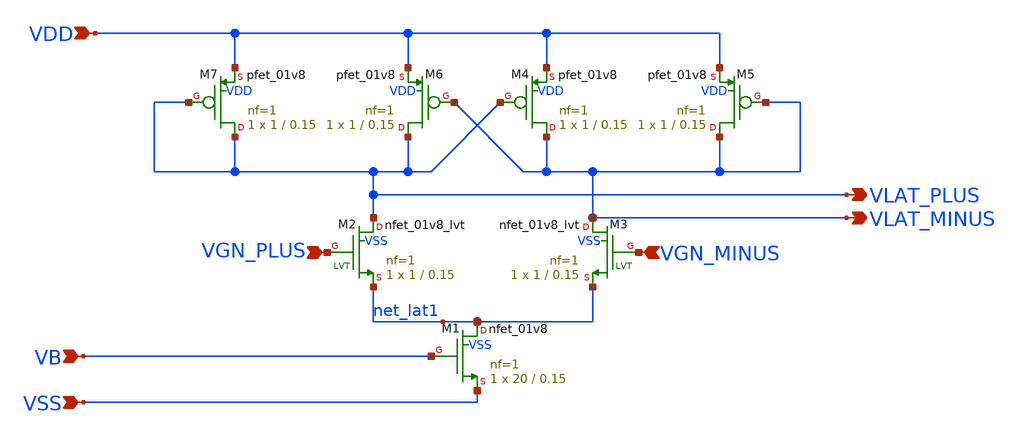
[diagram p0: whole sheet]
** sch_path: xschem/latch.sch
**.subckt latch VDD VSS VGN_PLUS VGN_MINUS VB VLAT_PLUS VLAT_MINUS
*.ipin VDD
*.ipin VSS
*.ipin VGN_PLUS
*.ipin VGN_MINUS
*.ipin VB
*.opin VLAT_PLUS
*.opin VLAT_MINUS
XM1 net_lat1 VB VSS VSS sky130_fd_pr__nfet_01v8 L=0.15 W=20 nf=1 ad='int((nf+1)/2) * W/nf * 0.29' as='int((nf+2)/2) * W/nf * 0.29'
+ pd='2*int((nf+1)/2) * (W/nf + 0.29)' ps='2*int((nf+2)/2) * (W/nf + 0.29)' nrd='0.29 / W' nrs='0.29 / W'
+ sa=0 sb=0 sd=0 mult=1 m=1
XM2 VLAT_PLUS VGN_PLUS net_lat1 VSS sky130_fd_pr__nfet_01v8_lvt L=0.15 W=1 nf=1 ad='int((nf+1)/2) * W/nf * 0.29'
+ as='int((nf+2)/2) * W/nf * 0.29' pd='2*int((nf+1)/2) * (W/nf + 0.29)' ps='2*int((nf+2)/2) * (W/nf + 0.29)'
+ nrd='0.29 / W' nrs='0.29 / W' sa=0 sb=0 sd=0 mult=1 m=1
XM3 VLAT_MINUS VGN_MINUS net_lat1 VSS sky130_fd_pr__nfet_01v8_lvt L=0.15 W=1 nf=1 ad='int((nf+1)/2) * W/nf * 0.29'
+ as='int((nf+2)/2) * W/nf * 0.29' pd='2*int((nf+1)/2) * (W/nf + 0.29)' ps='2*int((nf+2)/2) * (W/nf + 0.29)'
+ nrd='0.29 / W' nrs='0.29 / W' sa=0 sb=0 sd=0 mult=1 m=1
XM4 VLAT_MINUS VLAT_PLUS VDD VDD sky130_fd_pr__pfet_01v8 L=0.15 W=1 nf=1 ad='int((nf+1)/2) * W/nf * 0.29'
+ as='int((nf+2)/2) * W/nf * 0.29' pd='2*int((nf+1)/2) * (W/nf + 0.29)' ps='2*int((nf+2)/2) * (W/nf + 0.29)'
+ nrd='0.29 / W' nrs='0.29 / W' sa=0 sb=0 sd=0 mult=1 m=1
XM5 VLAT_MINUS VLAT_MINUS VDD VDD sky130_fd_pr__pfet_01v8 L=0.15 W=1 nf=1 ad='int((nf+1)/2) * W/nf * 0.29'
+ as='int((nf+2)/2) * W/nf * 0.29' pd='2*int((nf+1)/2) * (W/nf + 0.29)' ps='2*int((nf+2)/2) * (W/nf + 0.29)'
+ nrd='0.29 / W' nrs='0.29 / W' sa=0 sb=0 sd=0 mult=1 m=1
XM6 VLAT_PLUS VLAT_MINUS VDD VDD sky130_fd_pr__pfet_01v8 L=0.15 W=1 nf=1 ad='int((nf+1)/2) * W/nf * 0.29'
+ as='int((nf+2)/2) * W/nf * 0.29' pd='2*int((nf+1)/2) * (W/nf + 0.29)' ps='2*int((nf+2)/2) * (W/nf + 0.29)'
+ nrd='0.29 / W' nrs='0.29 / W' sa=0 sb=0 sd=0 mult=1 m=1
XM7 VLAT_PLUS VLAT_PLUS VDD VDD sky130_fd_pr__pfet_01v8 L=0.15 W=1 nf=1 ad='int((nf+1)/2) * W/nf * 0.29'
+ as='int((nf+2)/2) * W/nf * 0.29' pd='2*int((nf+1)/2) * (W/nf + 0.29)' ps='2*int((nf+2)/2) * (W/nf + 0.29)'
+ nrd='0.29 / W' nrs='0.29 / W' sa=0 sb=0 sd=0 mult=1 m=1
**.ends
.end
